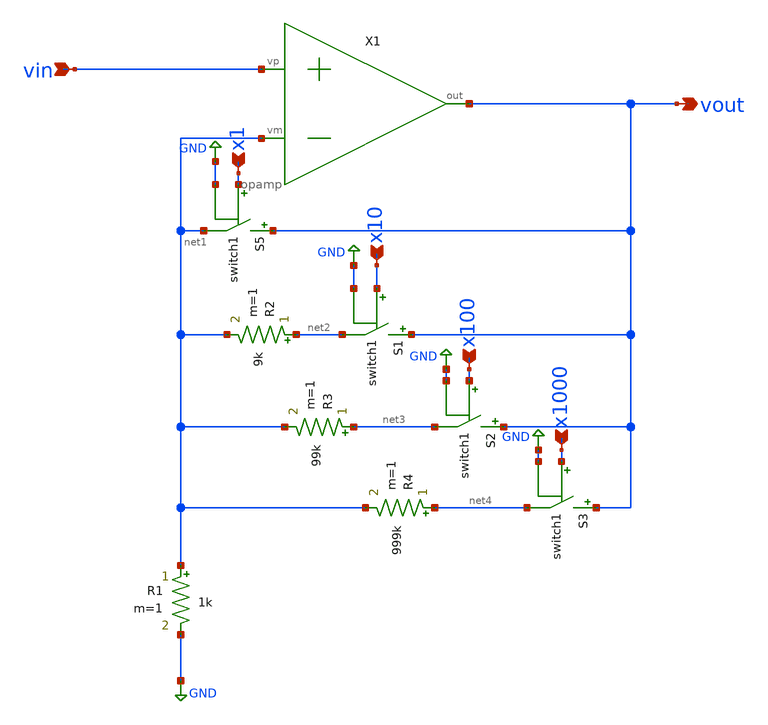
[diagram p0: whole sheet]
** sch_path: xschem/VGA/ideal_VGA.sch
**.subckt ideal_VGA vin x1 x10 x100 x1000 vout
*.ipin vin
*.ipin x1
*.ipin x10
*.ipin x100
*.ipin x1000
*.opin vout
X1 vin net1 vout opamp
R1 net1 GND 1k m=1
R2 net2 net1 9k m=1
R3 net3 net1 99k m=1
R4 net4 net1 999k m=1
S5 vout net1 x1 GND switch1 OFF
S1 vout net2 x10 GND switch1 OFF
S2 vout net3 x100 GND switch1 OFF
S3 vout net4 x1000 GND switch1 OFF
**.ends

* expanding   symbol:  MISC/opamp.sym # of pins=3
** sym_path: xschem/MISC/opamp.sym
** sch_path: xschem/MISC/opamp.sch
.subckt opamp vp vm out
*.ipin vp
*.ipin vm
*.opin out
E1 out GND vp vm 1E6
.ends

.GLOBAL GND
.end
